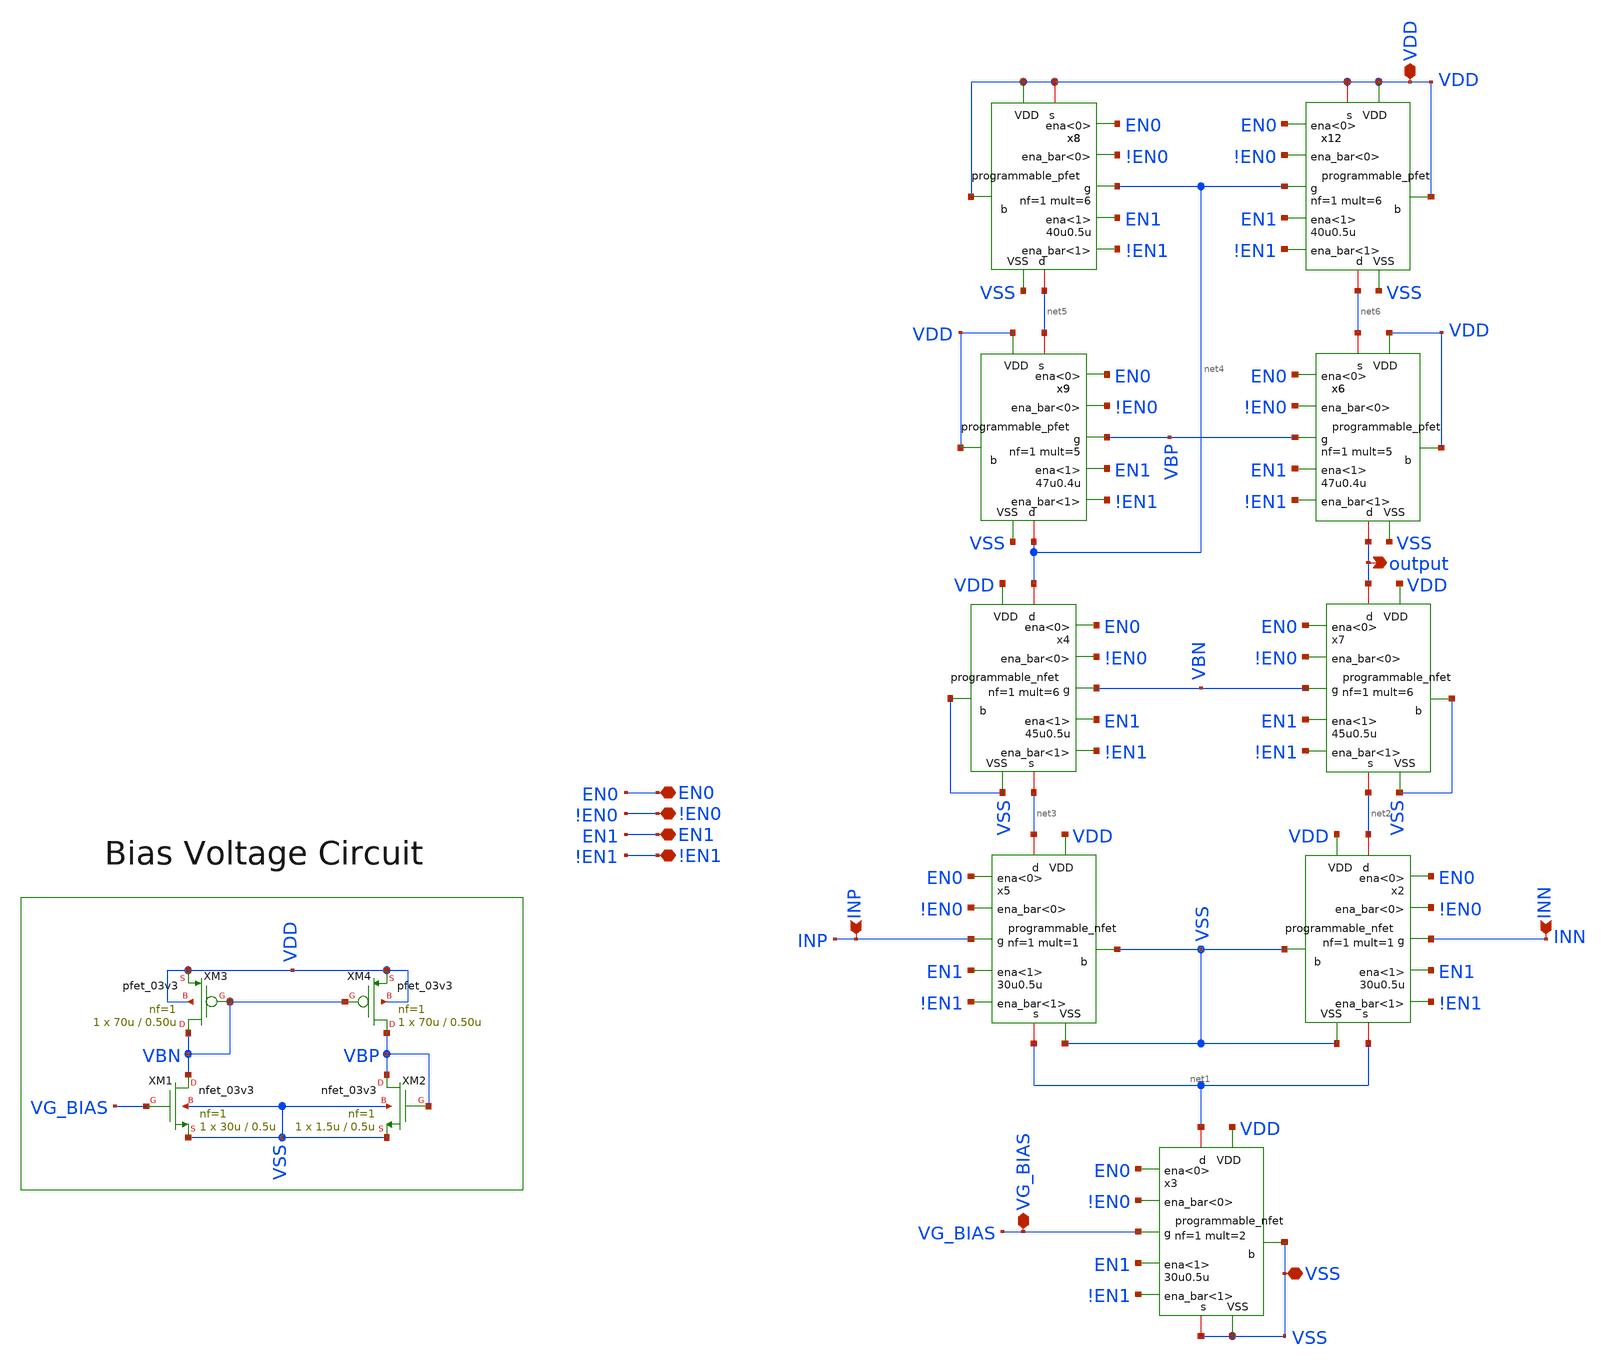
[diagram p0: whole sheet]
** sch_path: designs/libs/core_amps/ota_telescopic/programmable_ota_telescopic schematics/programmable_telescopic_cascode.sch
**.subckt programmable_telescopic_cascode output VDD !EN0 EN1 EN0 !EN1 INP INN VSS VG_BIAS
*.opin output
*.iopin VDD
*.iopin !EN0
*.iopin EN1
*.iopin EN0
*.iopin !EN1
*.ipin INP
*.ipin INN
*.iopin VSS
*.iopin VG_BIAS
XM1 VBN VG_BIAS VSS VSS nfet_03v3 L=0.5u W=30u nf=1 ad='int((nf+1)/2) * W/nf * 0.18u' as='int((nf+2)/2) * W/nf * 0.18u'
+ pd='2*int((nf+1)/2) * (W/nf + 0.18u)' ps='2*int((nf+2)/2) * (W/nf + 0.18u)' nrd='0.18u / W' nrs='0.18u / W'
+ sa=0 sb=0 sd=0 m=1
XM2 VBP VBP VSS VSS nfet_03v3 L=0.5u W=1.5u nf=1 ad='int((nf+1)/2) * W/nf * 0.18u' as='int((nf+2)/2) * W/nf * 0.18u'
+ pd='2*int((nf+1)/2) * (W/nf + 0.18u)' ps='2*int((nf+2)/2) * (W/nf + 0.18u)' nrd='0.18u / W' nrs='0.18u / W'
+ sa=0 sb=0 sd=0 m=1
XM4 VBP VBN VDD VDD pfet_03v3 L=0.50u W=70u nf=1 ad='int((nf+1)/2) * W/nf * 0.18u' as='int((nf+2)/2) * W/nf * 0.18u'
+ pd='2*int((nf+1)/2) * (W/nf + 0.18u)' ps='2*int((nf+2)/2) * (W/nf + 0.18u)' nrd='0.18u / W' nrs='0.18u / W'
+ sa=0 sb=0 sd=0 m=1
XM3 VBN VBN VDD VDD pfet_03v3 L=0.50u W=70u nf=1 ad='int((nf+1)/2) * W/nf * 0.18u' as='int((nf+2)/2) * W/nf * 0.18u'
+ pd='2*int((nf+1)/2) * (W/nf + 0.18u)' ps='2*int((nf+2)/2) * (W/nf + 0.18u)' nrd='0.18u / W' nrs='0.18u / W'
+ sa=0 sb=0 sd=0 m=1
x12 net6 VDD net4 VDD !EN0 VDD !EN1 EN0 EN1 VSS programmable_pfet width=40u length=0.5u nf=1 mult=6
x8 net5 VDD net4 VDD !EN0 VDD !EN1 EN0 EN1 VSS programmable_pfet width=40u length=0.5u nf=1 mult=6
x9 net4 VDD VBP net5 !EN0 VDD !EN1 EN0 EN1 VSS programmable_pfet width=47u length=0.4u nf=1 mult=5
x6 output VDD VBP net6 !EN0 VDD !EN1 EN0 EN1 VSS programmable_pfet width=47u length=0.4u nf=1 mult=5
x7 output VSS VBN net2 !EN0 VDD !EN1 EN0 EN1 VSS programmable_nfet width=45u length=0.5u nf=1 mult=6
x4 net4 VSS VBN net3 !EN0 VDD !EN1 EN0 EN1 VSS programmable_nfet width=45u length=0.5u nf=1 mult=6
x5 net3 VSS INP net1 !EN0 VDD !EN1 EN0 EN1 VSS programmable_nfet width=30u length=0.5u nf=1 mult=1
x2 net2 VSS INN net1 !EN0 VDD !EN1 EN0 EN1 VSS programmable_nfet width=30u length=0.5u nf=1 mult=1
x3 net1 VSS VG_BIAS VSS !EN0 VDD !EN1 EN0 EN1 VSS programmable_nfet width=30u length=0.5u nf=1
+ mult=2
**** begin user architecture code


.include /foss/pdks/gf180mcuD/libs.tech/ngspice/design.ngspice
.lib /foss/pdks/gf180mcuD/libs.tech/ngspice/sm141064.ngspice typical

**** end user architecture code
**.ends

* expanding   symbol:  libs/core_digital/schem/programmable_pfet.sym # of pins=10
** sym_path: designs/libs/core_digital/schem/programmable_pfet.sym
** sch_path: designs/libs/core_digital/schem/programmable_pfet.sch
.subckt programmable_pfet d b g s ena_bar<0> VDD ena_bar<1> ena<0> ena<1> VSS  width=0.22u
+ length=0.28u nf=1 mult=1
*.ipin VSS
*.ipin VDD
*.ipin g
*.ipin ena_bar<1>
*.ipin ena_bar<0>
*.ipin ena<0>
*.iopin s
*.iopin d
*.ipin b
*.ipin ena<1>
XM1 d net2 s b pfet_03v3 L={length} W={width} nf={nf} ad='int((nf+1)/2) * W/nf * 0.18u' as='int((nf+2)/2) * W/nf * 0.18u'
+ pd='2*int((nf+1)/2) * (W/nf + 0.18u)' ps='2*int((nf+2)/2) * (W/nf + 0.18u)' nrd='0.18u / W' nrs='0.18u / W'
+ sa=0 sb=0 sd=0 m={mult}
XM3 d net1 s b pfet_03v3 L={length} W={2*width} nf={2*nf} ad='int((nf+1)/2) * W/nf * 0.18u' as='int((nf+2)/2) * W/nf * 0.18u'
+ pd='2*int((nf+1)/2) * (W/nf + 0.18u)' ps='2*int((nf+2)/2) * (W/nf + 0.18u)' nrd='0.18u / W' nrs='0.18u / W'
+ sa=0 sb=0 sd=0 m={mult}
XM2 net1 ena<1> VDD VDD pfet_03v3 L=0.28u W=0.22u nf=1 ad='int((nf+1)/2) * W/nf * 0.18u' as='int((nf+2)/2) * W/nf * 0.18u'
+ pd='2*int((nf+1)/2) * (W/nf + 0.18u)' ps='2*int((nf+2)/2) * (W/nf + 0.18u)' nrd='0.18u / W' nrs='0.18u / W'
+ sa=0 sb=0 sd=0 m=1
XM4 net2 ena<0> VDD VDD pfet_03v3 L=0.28u W=0.22u nf=1 ad='int((nf+1)/2) * W/nf * 0.18u' as='int((nf+2)/2) * W/nf * 0.18u'
+ pd='2*int((nf+1)/2) * (W/nf + 0.18u)' ps='2*int((nf+2)/2) * (W/nf + 0.18u)' nrd='0.18u / W' nrs='0.18u / W'
+ sa=0 sb=0 sd=0 m=1
x1 ena_bar<0> VDD net2 g VSS ena<0> transmission_gate
x2 ena_bar<1> VDD net1 g VSS ena<1> transmission_gate
.ends


* expanding   symbol:  libs/core_digital/schem/programmable_nfet.sym # of pins=10
** sym_path: designs/libs/core_digital/schem/programmable_nfet.sym
** sch_path: designs/libs/core_digital/schem/programmable_nfet.sch
.subckt programmable_nfet d b g s ena_bar<0> VDD ena_bar<1> ena<0> ena<1> VSS  width=0.22u
+ length=0.28u nf=1 mult=1
*.ipin VSS
*.ipin VDD
*.ipin g
*.ipin ena_bar<1>
*.ipin ena_bar<0>
*.ipin ena<1>
*.ipin ena<0>
*.iopin d
*.iopin s
*.ipin b
XM1 d net2 s b nfet_03v3 L={length} W={width} nf={nf} ad='int((nf+1)/2) * W/nf * 0.18u' as='int((nf+2)/2) * W/nf * 0.18u'
+ pd='2*int((nf+1)/2) * (W/nf + 0.18u)' ps='2*int((nf+2)/2) * (W/nf + 0.18u)' nrd='0.18u / W' nrs='0.18u / W'
+ sa=0 sb=0 sd=0 m={mult}
XM3 d net1 s b nfet_03v3 L={length} W={2*width} nf={2*nf} ad='int((nf+1)/2) * W/nf * 0.18u' as='int((nf+2)/2) * W/nf * 0.18u'
+ pd='2*int((nf+1)/2) * (W/nf + 0.18u)' ps='2*int((nf+2)/2) * (W/nf + 0.18u)' nrd='0.18u / W' nrs='0.18u / W'
+ sa=0 sb=0 sd=0 m={mult}
XM2 net1 ena_bar<1> VSS VSS nfet_03v3 L=0.28u W=0.22u nf=1 ad='int((nf+1)/2) * W/nf * 0.18u' as='int((nf+2)/2) * W/nf * 0.18u'
+ pd='2*int((nf+1)/2) * (W/nf + 0.18u)' ps='2*int((nf+2)/2) * (W/nf + 0.18u)' nrd='0.18u / W' nrs='0.18u / W'
+ sa=0 sb=0 sd=0 m=1
XM4 net2 ena_bar<0> VSS VSS nfet_03v3 L=0.28u W=0.22u nf=1 ad='int((nf+1)/2) * W/nf * 0.18u' as='int((nf+2)/2) * W/nf * 0.18u'
+ pd='2*int((nf+1)/2) * (W/nf + 0.18u)' ps='2*int((nf+2)/2) * (W/nf + 0.18u)' nrd='0.18u / W' nrs='0.18u / W'
+ sa=0 sb=0 sd=0 m=1
x1 ena_bar<0> VDD net2 g VSS ena<0> transmission_gate
x2 ena_bar<1> VDD net1 g VSS ena<1> transmission_gate
.ends


* expanding   symbol:  libs/core_digital/schem/transmission_gate.sym # of pins=6
** sym_path: designs/libs/core_digital/schem/transmission_gate.sym
** sch_path: designs/libs/core_digital/schem/transmission_gate.sch
.subckt transmission_gate ena_bar VDD out in VSS ena
*.ipin in
*.ipin ena_bar
*.ipin ena
*.ipin VSS
*.ipin VDD
*.opin out
XM1 in ena_bar out VDD pfet_03v3 L=0.28u W=0.22u nf=1 ad='int((nf+1)/2) * W/nf * 0.18u' as='int((nf+2)/2) * W/nf * 0.18u'
+ pd='2*int((nf+1)/2) * (W/nf + 0.18u)' ps='2*int((nf+2)/2) * (W/nf + 0.18u)' nrd='0.18u / W' nrs='0.18u / W'
+ sa=0 sb=0 sd=0 m=1
XM2 in ena out VSS nfet_03v3 L=0.28u W=0.22u nf=1 ad='int((nf+1)/2) * W/nf * 0.18u' as='int((nf+2)/2) * W/nf * 0.18u'
+ pd='2*int((nf+1)/2) * (W/nf + 0.18u)' ps='2*int((nf+2)/2) * (W/nf + 0.18u)' nrd='0.18u / W' nrs='0.18u / W'
+ sa=0 sb=0 sd=0 m=1
.ends

.end
